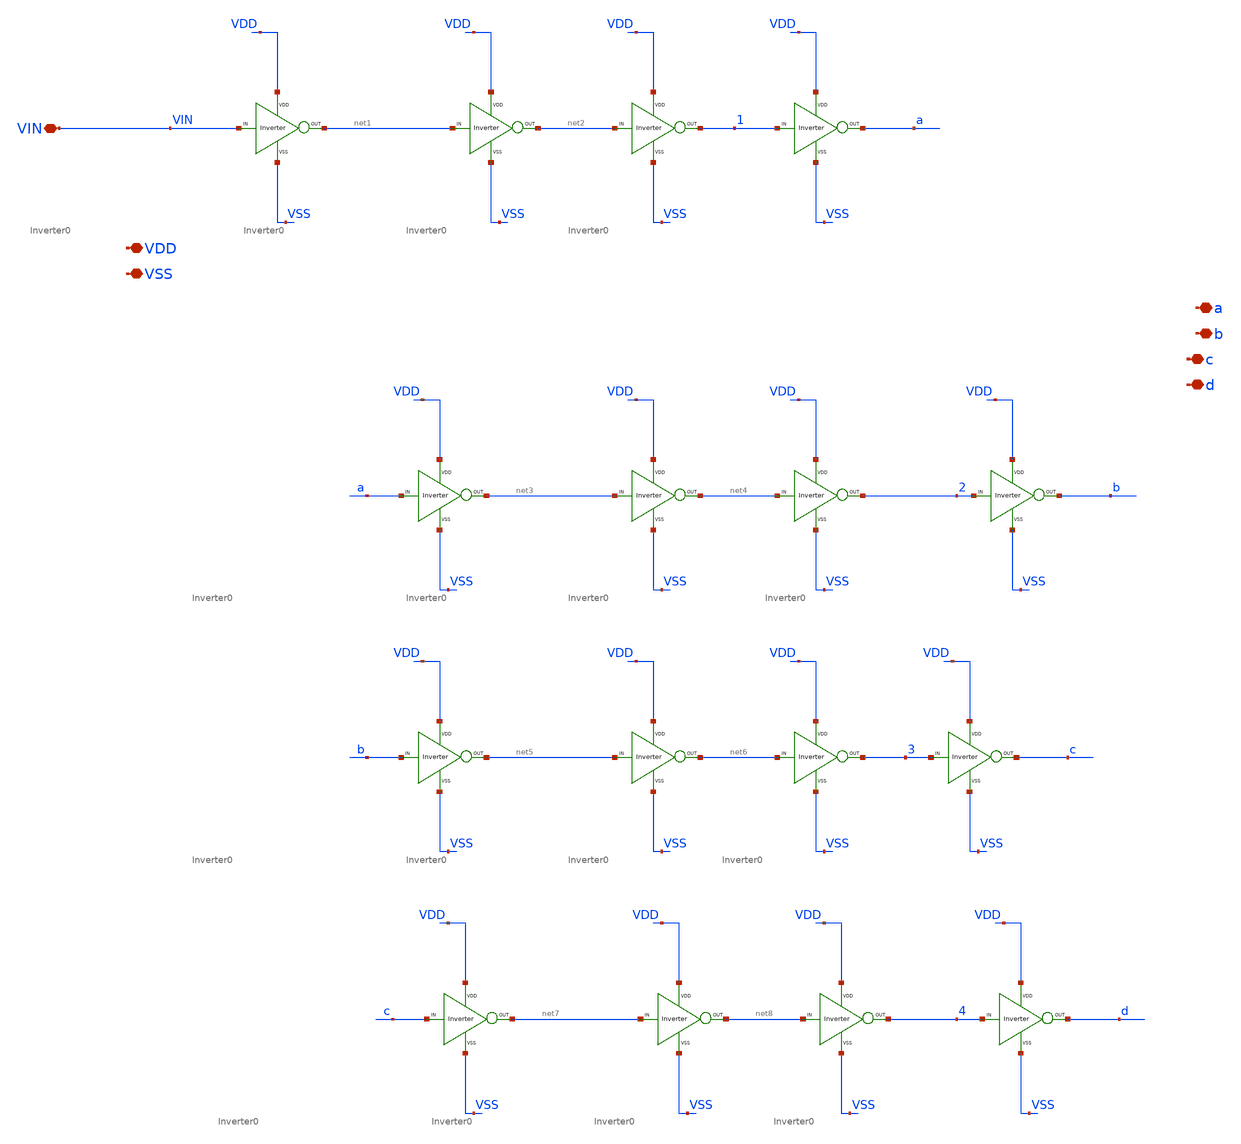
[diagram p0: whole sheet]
** sch_path: xschem/DC_DC_Converter_xschem/DC_DC_Converter/Delay_block_revised/delay_1_stage.sch
**.subckt delay_1_stage VDD VSS VIN a b c d
*.iopin VDD
*.iopin VSS
*.iopin VIN
*.iopin a
*.iopin b
*.iopin c
*.iopin d
X13 c net7 VDD VSS Inverter0
X10 net7 net8 VDD VSS Inverter0
X11 4 d VDD VSS Inverter0
X7 b net5 VDD VSS Inverter0
X8 net5 net6 VDD VSS Inverter0
X9 3 c VDD VSS Inverter0
X4 a net3 VDD VSS Inverter0
X5 net3 net4 VDD VSS Inverter0
X6 2 b VDD VSS Inverter0
X1 VIN net1 VDD VSS Inverter0
X2 net1 net2 VDD VSS Inverter0
X3 1 a VDD VSS Inverter0
X25 net2 1 VDD VSS Inverter0
X26 net4 2 VDD VSS Inverter0
X27 net6 3 VDD VSS Inverter0
X28 net8 4 VDD VSS Inverter0
**.ends

* expanding   symbol:  DC_DC_Converter/Delay_block_revised/Inverter_0/Inverter0.sym # of pins=4
** sym_path: xschem/DC_DC_Converter_xschem/DC_DC_Converter/Delay_block_revised/Inverter_0/Inverter0.sym
** sch_path: xschem/DC_DC_Converter_xschem/DC_DC_Converter/Delay_block_revised/Inverter_0/Inverter0.sch
.subckt Inverter0 VIN VOUT VDD VSS
*.ipin VIN
*.iopin VDD
*.iopin VSS
*.opin VOUT
XM1 VOUT VIN VSS VSS sky130_fd_pr__nfet_01v8 L=0.15 W=0.4 nf=1 ad='int((nf+1)/2) * W/nf * 0.29' as='int((nf+2)/2) * W/nf * 0.29'
+ pd='2*int((nf+1)/2) * (W/nf + 0.29)' ps='2*int((nf+2)/2) * (W/nf + 0.29)' nrd='0.29 / W' nrs='0.29 / W'
+ sa=0 sb=0 sd=0 mult=1 m=1
XM2 VOUT VIN VDD VDD sky130_fd_pr__pfet_01v8 L=0.15 W=1.2 nf=1 ad='int((nf+1)/2) * W/nf * 0.29' as='int((nf+2)/2) * W/nf * 0.29'
+ pd='2*int((nf+1)/2) * (W/nf + 0.29)' ps='2*int((nf+2)/2) * (W/nf + 0.29)' nrd='0.29 / W' nrs='0.29 / W'
+ sa=0 sb=0 sd=0 mult=1 m=1
.ends

.end
